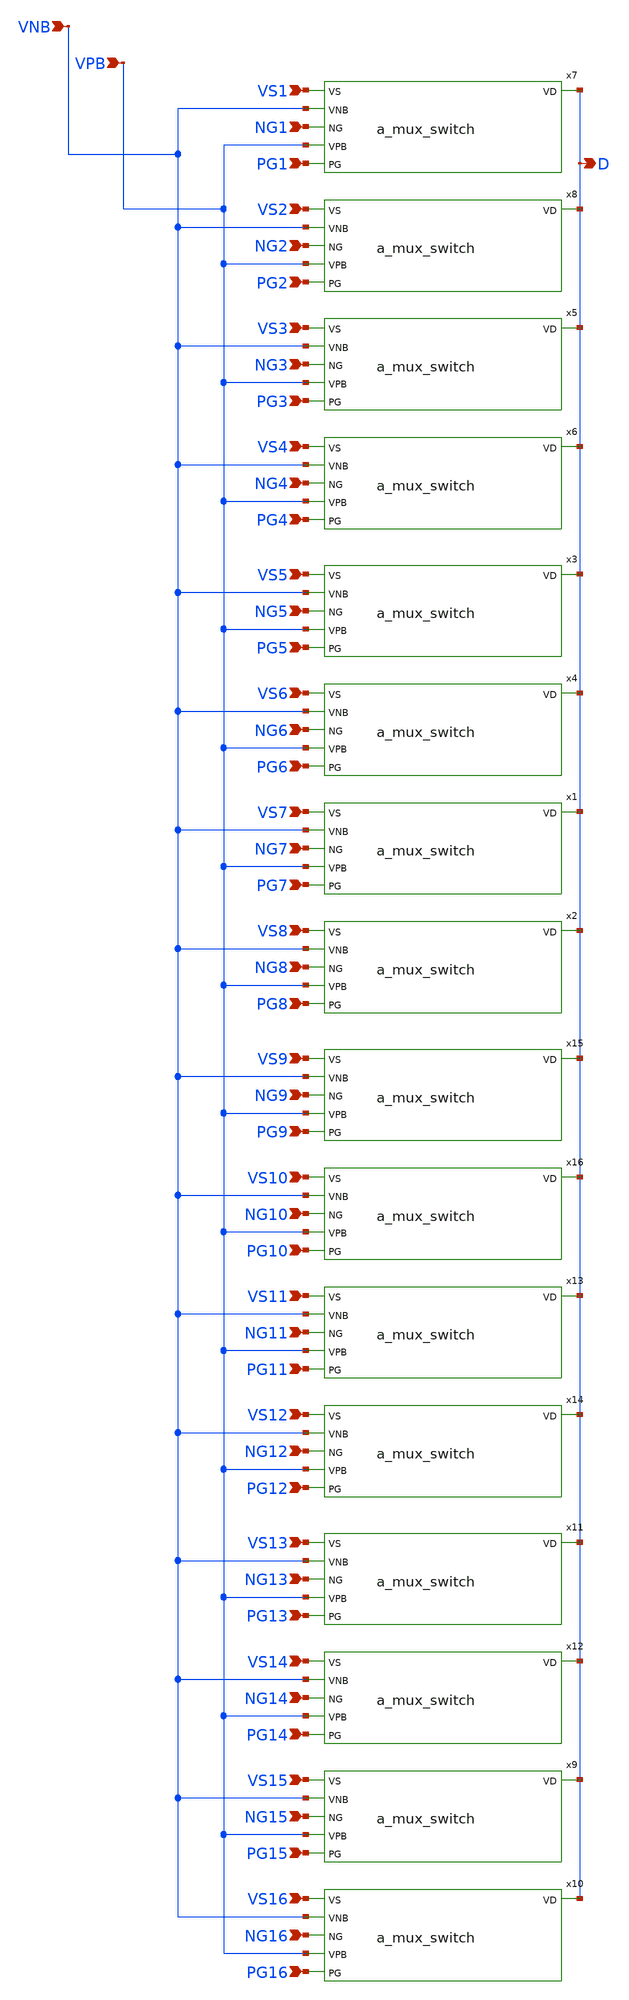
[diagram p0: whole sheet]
** sch_path: A_mux_switch_all.sch
**.subckt A_mux_switch_all D VS1 VS2 VS3 VS4 VS5 VS6 VS7 VS8 VS9 VS10 VS11 VS12 VS13 VS14 VS15 VS16
*+ VPB VNB NG1 PG1 NG2 PG2 NG3 PG3 NG4 PG4 NG5 PG5 NG6 PG6 NG7 PG7 NG8 PG8 NG9 PG9 NG10 PG10 NG11 PG11
*+ NG12 PG12 NG13 NG14 NG15 NG16 PG13 PG14 PG15 PG16
*.opin D
*.ipin VS1
*.ipin VS2
*.ipin VS3
*.ipin VS4
*.ipin VS5
*.ipin VS6
*.ipin VS7
*.ipin VS8
*.ipin VS9
*.ipin VS10
*.ipin VS11
*.ipin VS12
*.ipin VS13
*.ipin VS14
*.ipin VS15
*.ipin VS16
*.ipin VPB
*.ipin VNB
*.ipin NG1
*.ipin PG1
*.ipin NG2
*.ipin PG2
*.ipin NG3
*.ipin PG3
*.ipin NG4
*.ipin PG4
*.ipin NG5
*.ipin PG5
*.ipin NG6
*.ipin PG6
*.ipin NG7
*.ipin PG7
*.ipin NG8
*.ipin PG8
*.ipin NG9
*.ipin PG9
*.ipin NG10
*.ipin PG10
*.ipin NG11
*.ipin PG11
*.ipin NG12
*.ipin PG12
*.ipin NG13
*.ipin NG14
*.ipin NG15
*.ipin NG16
*.ipin PG13
*.ipin PG14
*.ipin PG15
*.ipin PG16
x1 VS7 VNB NG7 VPB PG7 D a_mux_switch
x2 VS8 VNB NG8 VPB PG8 D a_mux_switch
x3 VS5 VNB NG5 VPB PG5 D a_mux_switch
x4 VS6 VNB NG6 VPB PG6 D a_mux_switch
x5 VS3 VNB NG3 VPB PG3 D a_mux_switch
x6 VS4 VNB NG4 VPB PG4 D a_mux_switch
x7 VS1 VNB NG1 VPB PG1 D a_mux_switch
x8 VS2 VNB NG2 VPB PG2 D a_mux_switch
x9 VS15 VNB NG15 VPB PG15 D a_mux_switch
x10 VS16 VNB NG16 VPB PG16 D a_mux_switch
x11 VS13 VNB NG13 VPB PG13 D a_mux_switch
x12 VS14 VNB NG14 VPB PG14 D a_mux_switch
x13 VS11 VNB NG11 VPB PG11 D a_mux_switch
x14 VS12 VNB NG12 VPB PG12 D a_mux_switch
x15 VS9 VNB NG9 VPB PG9 D a_mux_switch
x16 VS10 VNB NG10 VPB PG10 D a_mux_switch
**.ends

* expanding   symbol:  compiled 2/a_mux_switch.sym # of pins=6
** sym_path: compiled 2/a_mux_switch.sym
** sch_path: compiled 2/a_mux_switch.sch
.subckt a_mux_switch VS VNB NG VPB PG VD
*.ipin PG
*.ipin NG
*.ipin VS
*.opin VD
*.ipin VPB
*.ipin VNB
XM1 VD PG VS VPB sky130_fd_pr__pfet_01v8 L=0.15 W=60 nf=1 ad='int((nf+1)/2) * W/nf * 0.29' as='int((nf+2)/2) * W/nf * 0.29'
+ pd='2*int((nf+1)/2) * (W/nf + 0.29)' ps='2*int((nf+2)/2) * (W/nf + 0.29)' nrd='0.29 / W' nrs='0.29 / W'
+ sa=0 sb=0 sd=0 mult=1 m=1
XM2 VD NG VS VNB sky130_fd_pr__nfet_01v8 L=0.15 W=40 nf=1 ad='int((nf+1)/2) * W/nf * 0.29' as='int((nf+2)/2) * W/nf * 0.29'
+ pd='2*int((nf+1)/2) * (W/nf + 0.29)' ps='2*int((nf+2)/2) * (W/nf + 0.29)' nrd='0.29 / W' nrs='0.29 / W'
+ sa=0 sb=0 sd=0 mult=1 m=1
.ends

.end
